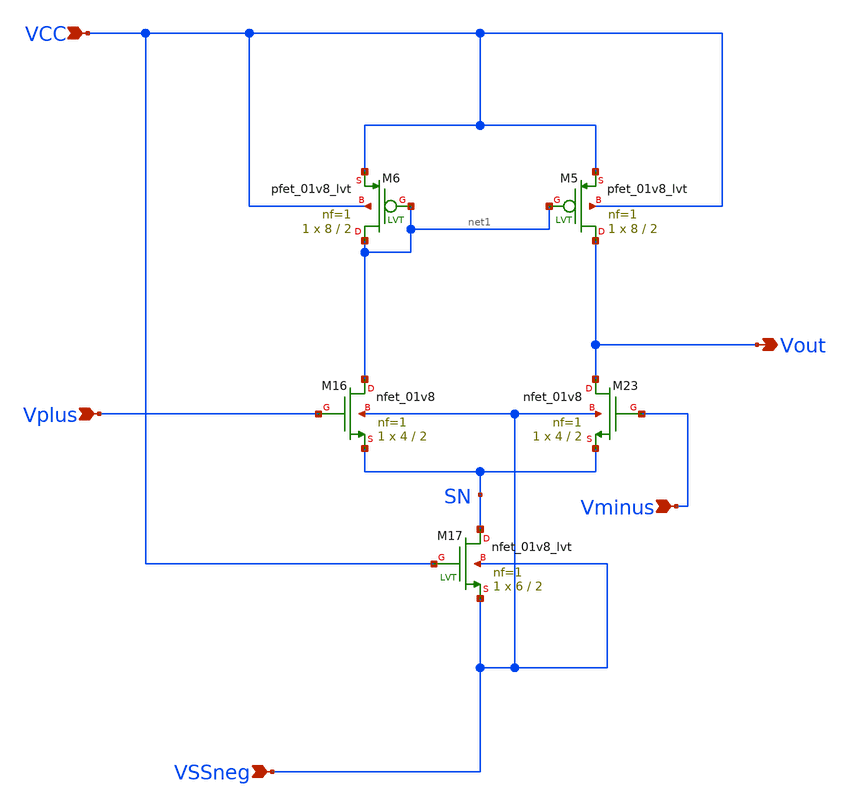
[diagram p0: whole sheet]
** sch_path: xschem/OpAmp5TNeg.sch
**.subckt OpAmp5TNeg VCC VSSneg Vplus Vminus Vout
*.ipin VCC
*.ipin VSSneg
*.ipin Vplus
*.ipin Vminus
*.opin Vout
XM5 Vout net1 VCC VCC sky130_fd_pr__pfet_01v8_lvt L=2 W=8 nf=1 ad='W * 0.29' as='W * 0.29' pd='2*(W + 0.29)'
+ ps='2*(W + 0.29)' nrd=0 nrs=0 sa=0 sb=0 sd=0 mult=1 m=1
XM6 net1 net1 VCC VCC sky130_fd_pr__pfet_01v8_lvt L=2 W=8 nf=1 ad='W * 0.29' as='W * 0.29' pd='2*(W + 0.29)'
+ ps='2*(W + 0.29)' nrd=0 nrs=0 sa=0 sb=0 sd=0 mult=1 m=1
XM17 SN VCC VSSneg VSSneg sky130_fd_pr__nfet_01v8_lvt L=2 W=6 nf=1 ad='W * 0.29' as='W * 0.29' pd='2*(W + 0.29)'
+ ps='2*(W + 0.29)' nrd=0 nrs=0 sa=0 sb=0 sd=0 mult=1 m=1
XM23 Vout Vminus SN VSSneg sky130_fd_pr__nfet_01v8 L=2 W=4 nf=1 ad='W * 0.29' as='W * 0.29' pd='2*(W + 0.29)'
+ ps='2*(W + 0.29)' nrd=0 nrs=0 sa=0 sb=0 sd=0 mult=1 m=1
XM16 net1 Vplus SN VSSneg sky130_fd_pr__nfet_01v8 L=2 W=4 nf=1 ad='W * 0.29' as='W * 0.29' pd='2*(W + 0.29)'
+ ps='2*(W + 0.29)' nrd=0 nrs=0 sa=0 sb=0 sd=0 mult=1 m=1
**.ends
.end
